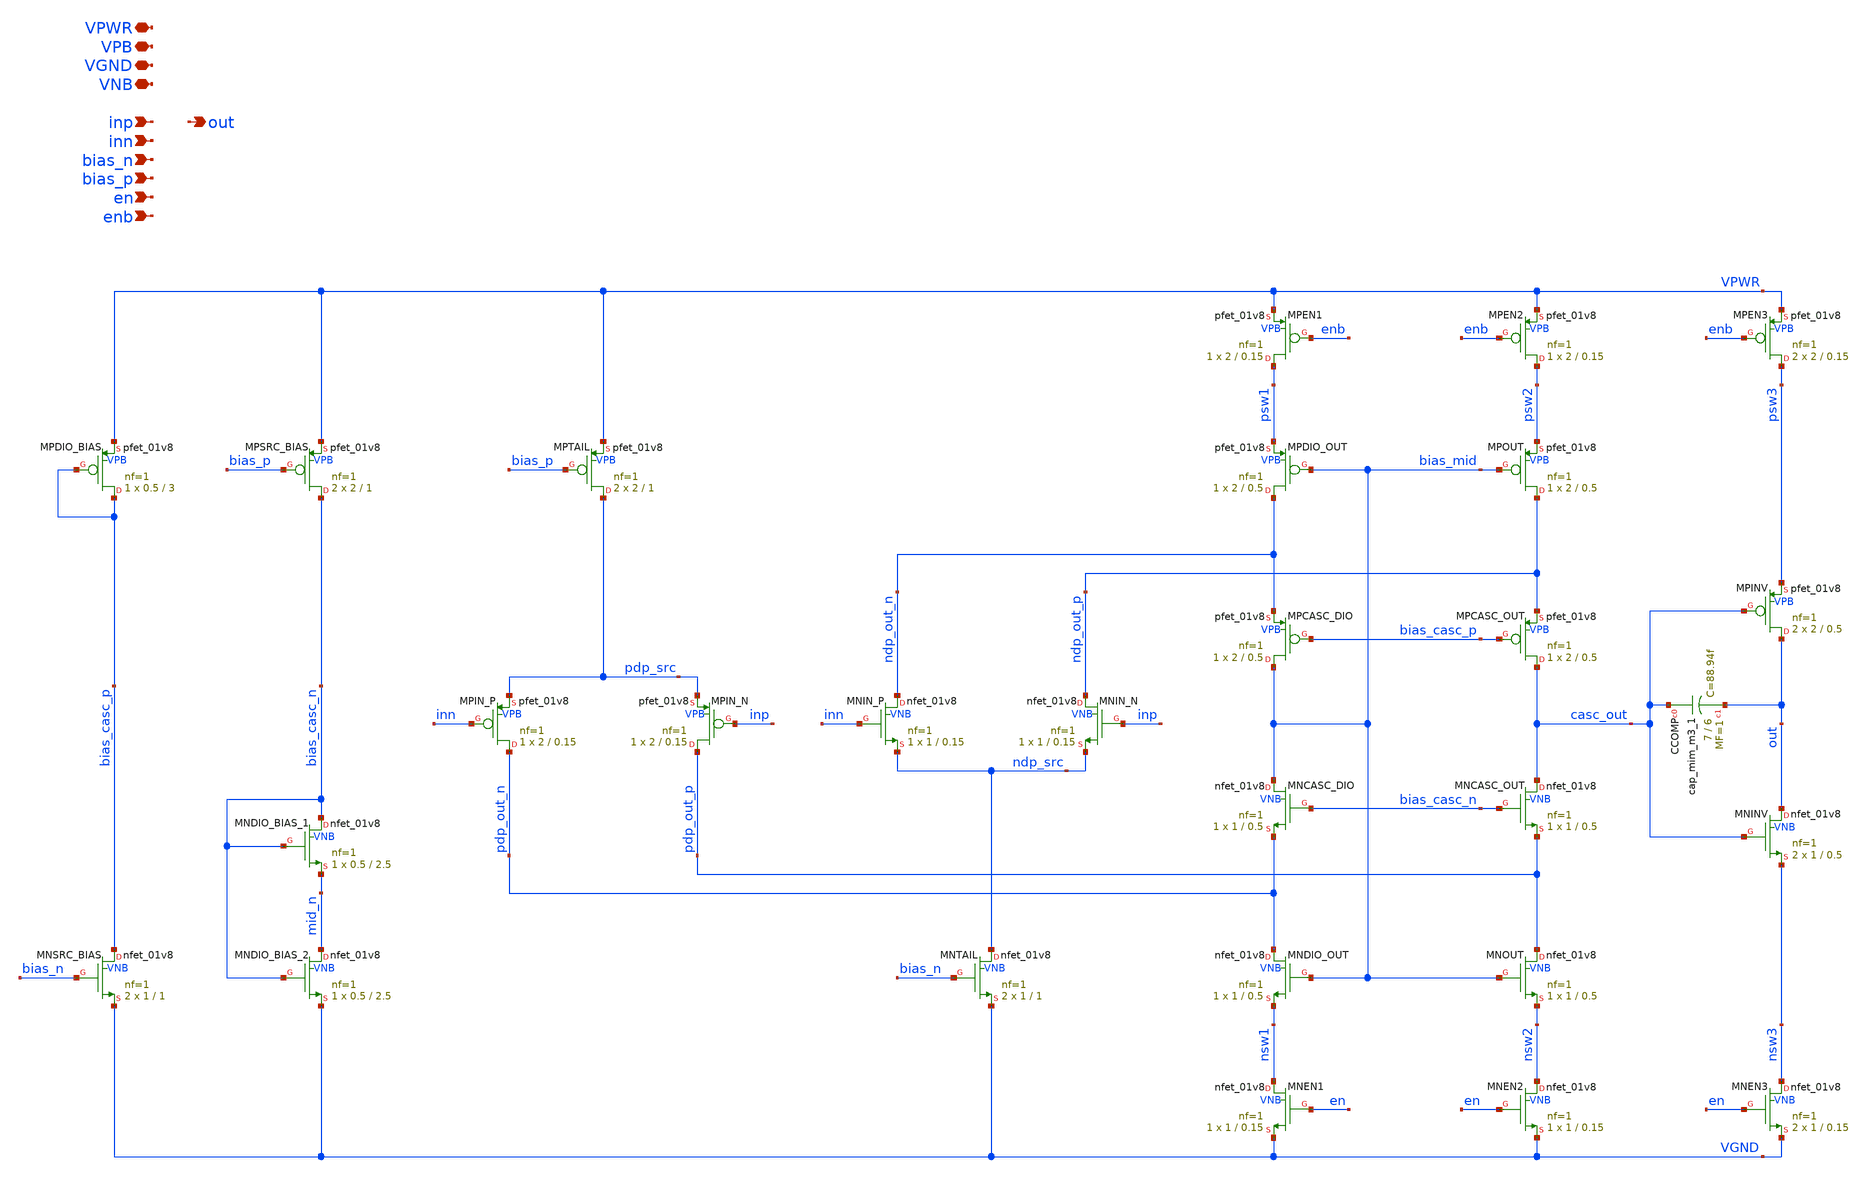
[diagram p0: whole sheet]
** sch_path: xschem/tiny_adc/tiny_adc_opamp.sch
**.subckt tiny_adc_opamp VPWR VPB VGND VNB inp out inn bias_n bias_p en enb
*.iopin VPWR
*.iopin VPB
*.iopin VGND
*.iopin VNB
*.ipin inp
*.opin out
*.ipin inn
*.ipin bias_n
*.ipin bias_p
*.ipin en
*.ipin enb
XMNDIO_OUT pdp_out_n bias_mid nsw1 VNB sky130_fd_pr__nfet_01v8 L=0.5 W=1 nf=1 ad='int((nf+1)/2) * W/nf * 0.29'
+ as='int((nf+2)/2) * W/nf * 0.29' pd='2*int((nf+1)/2) * (W/nf + 0.29)' ps='2*int((nf+2)/2) * (W/nf + 0.29)'
+ nrd='0.29 / W' nrs='0.29 / W' sa=0 sb=0 sd=0 mult=1 m=1
XMNOUT pdp_out_p bias_mid nsw2 VNB sky130_fd_pr__nfet_01v8 L=0.5 W=1 nf=1 ad='int((nf+1)/2) * W/nf * 0.29'
+ as='int((nf+2)/2) * W/nf * 0.29' pd='2*int((nf+1)/2) * (W/nf + 0.29)' ps='2*int((nf+2)/2) * (W/nf + 0.29)'
+ nrd='0.29 / W' nrs='0.29 / W' sa=0 sb=0 sd=0 mult=1 m=1
XMNCASC_DIO bias_mid bias_casc_n pdp_out_n VNB sky130_fd_pr__nfet_01v8 L=0.5 W=1 nf=1 ad='int((nf+1)/2) * W/nf * 0.29'
+ as='int((nf+2)/2) * W/nf * 0.29' pd='2*int((nf+1)/2) * (W/nf + 0.29)' ps='2*int((nf+2)/2) * (W/nf + 0.29)'
+ nrd='0.29 / W' nrs='0.29 / W' sa=0 sb=0 sd=0 mult=1 m=1
XMNCASC_OUT casc_out bias_casc_n pdp_out_p VNB sky130_fd_pr__nfet_01v8 L=0.5 W=1 nf=1 ad='int((nf+1)/2) * W/nf * 0.29'
+ as='int((nf+2)/2) * W/nf * 0.29' pd='2*int((nf+1)/2) * (W/nf + 0.29)' ps='2*int((nf+2)/2) * (W/nf + 0.29)'
+ nrd='0.29 / W' nrs='0.29 / W' sa=0 sb=0 sd=0 mult=1 m=1
XMPCASC_DIO bias_mid bias_casc_p ndp_out_n VPB sky130_fd_pr__pfet_01v8 L=0.5 W=2 nf=1 ad='int((nf+1)/2) * W/nf * 0.29'
+ as='int((nf+2)/2) * W/nf * 0.29' pd='2*int((nf+1)/2) * (W/nf + 0.29)' ps='2*int((nf+2)/2) * (W/nf + 0.29)'
+ nrd='0.29 / W' nrs='0.29 / W' sa=0 sb=0 sd=0 mult=1 m=1
XMPCASC_OUT casc_out bias_casc_p ndp_out_p VPB sky130_fd_pr__pfet_01v8 L=0.5 W=2 nf=1 ad='int((nf+1)/2) * W/nf * 0.29'
+ as='int((nf+2)/2) * W/nf * 0.29' pd='2*int((nf+1)/2) * (W/nf + 0.29)' ps='2*int((nf+2)/2) * (W/nf + 0.29)'
+ nrd='0.29 / W' nrs='0.29 / W' sa=0 sb=0 sd=0 mult=1 m=1
XMPDIO_OUT ndp_out_n bias_mid psw1 VPB sky130_fd_pr__pfet_01v8 L=0.5 W=2 nf=1 ad='int((nf+1)/2) * W/nf * 0.29'
+ as='int((nf+2)/2) * W/nf * 0.29' pd='2*int((nf+1)/2) * (W/nf + 0.29)' ps='2*int((nf+2)/2) * (W/nf + 0.29)'
+ nrd='0.29 / W' nrs='0.29 / W' sa=0 sb=0 sd=0 mult=1 m=1
XMPOUT ndp_out_p bias_mid psw2 VPB sky130_fd_pr__pfet_01v8 L=0.5 W=2 nf=1 ad='int((nf+1)/2) * W/nf * 0.29'
+ as='int((nf+2)/2) * W/nf * 0.29' pd='2*int((nf+1)/2) * (W/nf + 0.29)' ps='2*int((nf+2)/2) * (W/nf + 0.29)'
+ nrd='0.29 / W' nrs='0.29 / W' sa=0 sb=0 sd=0 mult=1 m=1
XMNIN_P ndp_out_n inn ndp_src VNB sky130_fd_pr__nfet_01v8 L=0.15 W=1 nf=1 ad='int((nf+1)/2) * W/nf * 0.29'
+ as='int((nf+2)/2) * W/nf * 0.29' pd='2*int((nf+1)/2) * (W/nf + 0.29)' ps='2*int((nf+2)/2) * (W/nf + 0.29)'
+ nrd='0.29 / W' nrs='0.29 / W' sa=0 sb=0 sd=0 mult=1 m=1
XMNIN_N ndp_out_p inp ndp_src VNB sky130_fd_pr__nfet_01v8 L=0.15 W=1 nf=1 ad='int((nf+1)/2) * W/nf * 0.29'
+ as='int((nf+2)/2) * W/nf * 0.29' pd='2*int((nf+1)/2) * (W/nf + 0.29)' ps='2*int((nf+2)/2) * (W/nf + 0.29)'
+ nrd='0.29 / W' nrs='0.29 / W' sa=0 sb=0 sd=0 mult=1 m=1
XMNTAIL ndp_src bias_n VGND VNB sky130_fd_pr__nfet_01v8 L=1 W=1 nf=1 ad='int((nf+1)/2) * W/nf * 0.29'
+ as='int((nf+2)/2) * W/nf * 0.29' pd='2*int((nf+1)/2) * (W/nf + 0.29)' ps='2*int((nf+2)/2) * (W/nf + 0.29)'
+ nrd='0.29 / W' nrs='0.29 / W' sa=0 sb=0 sd=0 mult=2 m=2
XMPIN_N pdp_out_p inp pdp_src VPB sky130_fd_pr__pfet_01v8 L=0.15 W=2 nf=1 ad='int((nf+1)/2) * W/nf * 0.29'
+ as='int((nf+2)/2) * W/nf * 0.29' pd='2*int((nf+1)/2) * (W/nf + 0.29)' ps='2*int((nf+2)/2) * (W/nf + 0.29)'
+ nrd='0.29 / W' nrs='0.29 / W' sa=0 sb=0 sd=0 mult=1 m=1
XMPIN_P pdp_out_n inn pdp_src VPB sky130_fd_pr__pfet_01v8 L=0.15 W=2 nf=1 ad='int((nf+1)/2) * W/nf * 0.29'
+ as='int((nf+2)/2) * W/nf * 0.29' pd='2*int((nf+1)/2) * (W/nf + 0.29)' ps='2*int((nf+2)/2) * (W/nf + 0.29)'
+ nrd='0.29 / W' nrs='0.29 / W' sa=0 sb=0 sd=0 mult=1 m=1
XMPTAIL pdp_src bias_p VPWR VPB sky130_fd_pr__pfet_01v8 L=1 W=2 nf=1 ad='int((nf+1)/2) * W/nf * 0.29'
+ as='int((nf+2)/2) * W/nf * 0.29' pd='2*int((nf+1)/2) * (W/nf + 0.29)' ps='2*int((nf+2)/2) * (W/nf + 0.29)'
+ nrd='0.29 / W' nrs='0.29 / W' sa=0 sb=0 sd=0 mult=2 m=2
XMPSRC_BIAS bias_casc_n bias_p VPWR VPB sky130_fd_pr__pfet_01v8 L=1 W=2 nf=1 ad='int((nf+1)/2) * W/nf * 0.29'
+ as='int((nf+2)/2) * W/nf * 0.29' pd='2*int((nf+1)/2) * (W/nf + 0.29)' ps='2*int((nf+2)/2) * (W/nf + 0.29)'
+ nrd='0.29 / W' nrs='0.29 / W' sa=0 sb=0 sd=0 mult=2 m=2
XMNSRC_BIAS bias_casc_p bias_n VGND VNB sky130_fd_pr__nfet_01v8 L=1 W=1 nf=1 ad='int((nf+1)/2) * W/nf * 0.29'
+ as='int((nf+2)/2) * W/nf * 0.29' pd='2*int((nf+1)/2) * (W/nf + 0.29)' ps='2*int((nf+2)/2) * (W/nf + 0.29)'
+ nrd='0.29 / W' nrs='0.29 / W' sa=0 sb=0 sd=0 mult=2 m=2
XMPDIO_BIAS bias_casc_p bias_casc_p VPWR VPB sky130_fd_pr__pfet_01v8 L=3 W=0.5 nf=1 ad='int((nf+1)/2) * W/nf * 0.29'
+ as='int((nf+2)/2) * W/nf * 0.29' pd='2*int((nf+1)/2) * (W/nf + 0.29)' ps='2*int((nf+2)/2) * (W/nf + 0.29)'
+ nrd='0.29 / W' nrs='0.29 / W' sa=0 sb=0 sd=0 mult=1 m=1
XMNINV out casc_out nsw3 VNB sky130_fd_pr__nfet_01v8 L=0.5 W=1 nf=1 ad='int((nf+1)/2) * W/nf * 0.29'
+ as='int((nf+2)/2) * W/nf * 0.29' pd='2*int((nf+1)/2) * (W/nf + 0.29)' ps='2*int((nf+2)/2) * (W/nf + 0.29)'
+ nrd='0.29 / W' nrs='0.29 / W' sa=0 sb=0 sd=0 mult=2 m=2
XMPINV out casc_out psw3 VPB sky130_fd_pr__pfet_01v8 L=0.5 W=2 nf=1 ad='int((nf+1)/2) * W/nf * 0.29'
+ as='int((nf+2)/2) * W/nf * 0.29' pd='2*int((nf+1)/2) * (W/nf + 0.29)' ps='2*int((nf+2)/2) * (W/nf + 0.29)'
+ nrd='0.29 / W' nrs='0.29 / W' sa=0 sb=0 sd=0 mult=2 m=2
XCCOMP casc_out out sky130_fd_pr__cap_mim_m3_1 W=7 L=6 MF=1 m=1
XMNEN1 nsw1 en VGND VNB sky130_fd_pr__nfet_01v8 L=0.15 W=1 nf=1 ad='int((nf+1)/2) * W/nf * 0.29' as='int((nf+2)/2) * W/nf * 0.29'
+ pd='2*int((nf+1)/2) * (W/nf + 0.29)' ps='2*int((nf+2)/2) * (W/nf + 0.29)' nrd='0.29 / W' nrs='0.29 / W'
+ sa=0 sb=0 sd=0 mult=1 m=1
XMNEN2 nsw2 en VGND VNB sky130_fd_pr__nfet_01v8 L=0.15 W=1 nf=1 ad='int((nf+1)/2) * W/nf * 0.29' as='int((nf+2)/2) * W/nf * 0.29'
+ pd='2*int((nf+1)/2) * (W/nf + 0.29)' ps='2*int((nf+2)/2) * (W/nf + 0.29)' nrd='0.29 / W' nrs='0.29 / W'
+ sa=0 sb=0 sd=0 mult=1 m=1
XMNEN3 nsw3 en VGND VNB sky130_fd_pr__nfet_01v8 L=0.15 W=1 nf=1 ad='int((nf+1)/2) * W/nf * 0.29' as='int((nf+2)/2) * W/nf * 0.29'
+ pd='2*int((nf+1)/2) * (W/nf + 0.29)' ps='2*int((nf+2)/2) * (W/nf + 0.29)' nrd='0.29 / W' nrs='0.29 / W'
+ sa=0 sb=0 sd=0 mult=2 m=2
XMPEN1 psw1 enb VPWR VPB sky130_fd_pr__pfet_01v8 L=0.15 W=2 nf=1 ad='int((nf+1)/2) * W/nf * 0.29' as='int((nf+2)/2) * W/nf * 0.29'
+ pd='2*int((nf+1)/2) * (W/nf + 0.29)' ps='2*int((nf+2)/2) * (W/nf + 0.29)' nrd='0.29 / W' nrs='0.29 / W'
+ sa=0 sb=0 sd=0 mult=1 m=1
XMPEN2 psw2 enb VPWR VPB sky130_fd_pr__pfet_01v8 L=0.15 W=2 nf=1 ad='int((nf+1)/2) * W/nf * 0.29' as='int((nf+2)/2) * W/nf * 0.29'
+ pd='2*int((nf+1)/2) * (W/nf + 0.29)' ps='2*int((nf+2)/2) * (W/nf + 0.29)' nrd='0.29 / W' nrs='0.29 / W'
+ sa=0 sb=0 sd=0 mult=1 m=1
XMPEN3 psw3 enb VPWR VPB sky130_fd_pr__pfet_01v8 L=0.15 W=2 nf=1 ad='int((nf+1)/2) * W/nf * 0.29' as='int((nf+2)/2) * W/nf * 0.29'
+ pd='2*int((nf+1)/2) * (W/nf + 0.29)' ps='2*int((nf+2)/2) * (W/nf + 0.29)' nrd='0.29 / W' nrs='0.29 / W'
+ sa=0 sb=0 sd=0 mult=2 m=2
XMNDIO_BIAS_2 mid_n bias_casc_n VGND VNB sky130_fd_pr__nfet_01v8 L=2.5 W=0.5 nf=1 ad='int((nf+1)/2) * W/nf * 0.29'
+ as='int((nf+2)/2) * W/nf * 0.29' pd='2*int((nf+1)/2) * (W/nf + 0.29)' ps='2*int((nf+2)/2) * (W/nf + 0.29)'
+ nrd='0.29 / W' nrs='0.29 / W' sa=0 sb=0 sd=0 mult=1 m=1
XMNDIO_BIAS_1 bias_casc_n bias_casc_n mid_n VNB sky130_fd_pr__nfet_01v8 L=2.5 W=0.5 nf=1 ad='int((nf+1)/2) * W/nf * 0.29'
+ as='int((nf+2)/2) * W/nf * 0.29' pd='2*int((nf+1)/2) * (W/nf + 0.29)' ps='2*int((nf+2)/2) * (W/nf + 0.29)'
+ nrd='0.29 / W' nrs='0.29 / W' sa=0 sb=0 sd=0 mult=1 m=1
**.ends
.end
